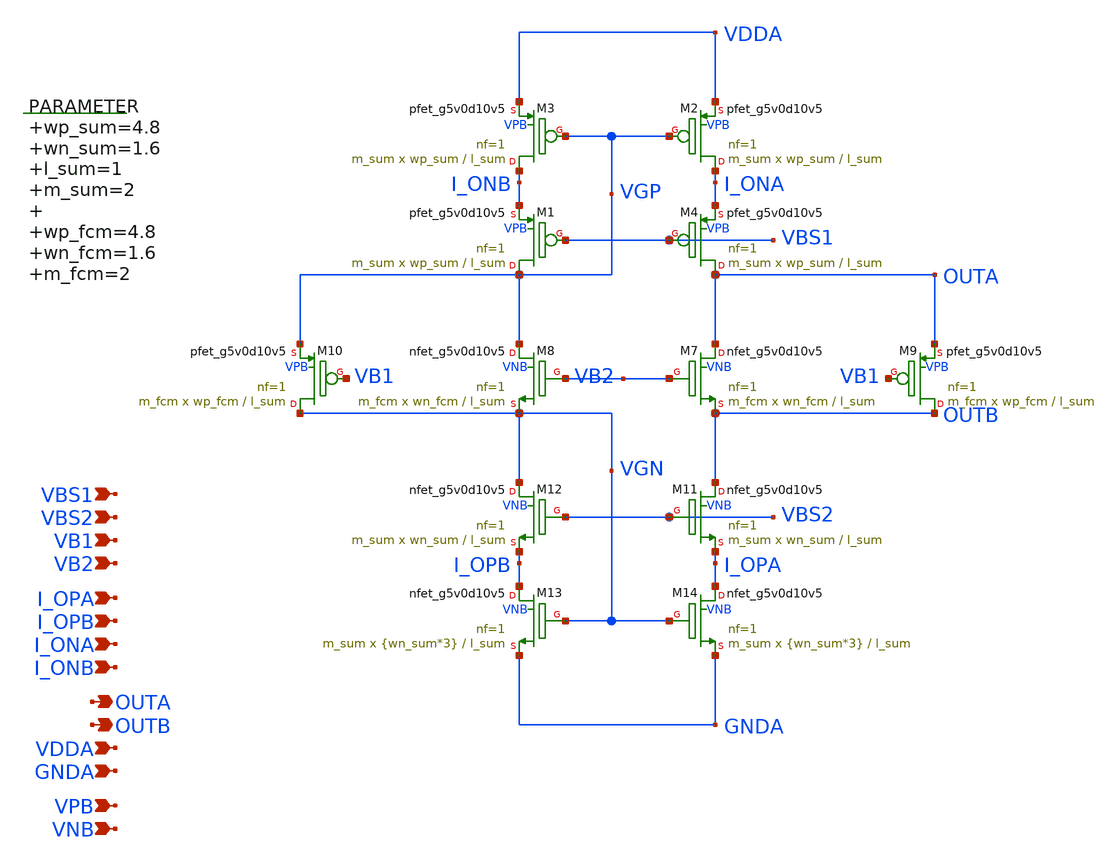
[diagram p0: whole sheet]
** sch_path: xschem/folded_cascode.sch
**.subckt folded_cascode I_OPA I_OPB I_ONA I_ONB OUTA OUTB VBS1 VBS2 VB1 VB2 VDDA VPB GNDA VNB
*.ipin I_OPA
*.ipin I_OPB
*.ipin I_ONA
*.ipin I_ONB
*.opin OUTA
*.opin OUTB
*.ipin VBS1
*.ipin VBS2
*.ipin VB1
*.ipin VB2
*.ipin VDDA
*.ipin VPB
*.ipin GNDA
*.ipin VNB
.param wp_sum=4.8 wn_sum=1.6 l_sum=1 m_sum=2 wp_fcm=4.8 wn_fcm=1.6 m_fcm=2

XM3 I_ONB VGP VDDA VPB sky130_fd_pr__pfet_g5v0d10v5 L=l_sum W=wp_sum nf=1 ad='int((nf+1)/2) * W/nf * 0.29'
+ as='int((nf+2)/2) * W/nf * 0.29' pd='2*int((nf+1)/2) * (W/nf + 0.29)' ps='2*int((nf+2)/2) * (W/nf + 0.29)'
+ nrd='0.29 / W' nrs='0.29 / W' sa=0 sb=0 sd=0 mult=m_sum m=m_sum
XM7 OUTA VB2 OUTB VNB sky130_fd_pr__nfet_g5v0d10v5 L=l_sum W=wn_fcm nf=1 ad='int((nf+1)/2) * W/nf * 0.29'
+ as='int((nf+2)/2) * W/nf * 0.29' pd='2*int((nf+1)/2) * (W/nf + 0.29)' ps='2*int((nf+2)/2) * (W/nf + 0.29)'
+ nrd='0.29 / W' nrs='0.29 / W' sa=0 sb=0 sd=0 mult=m_fcm m=m_fcm
XM8 VGP VB2 VGN VNB sky130_fd_pr__nfet_g5v0d10v5 L=l_sum W=wn_fcm nf=1 ad='int((nf+1)/2) * W/nf * 0.29'
+ as='int((nf+2)/2) * W/nf * 0.29' pd='2*int((nf+1)/2) * (W/nf + 0.29)' ps='2*int((nf+2)/2) * (W/nf + 0.29)'
+ nrd='0.29 / W' nrs='0.29 / W' sa=0 sb=0 sd=0 mult=m_fcm m=m_fcm
XM10 VGN VB1 VGP VPB sky130_fd_pr__pfet_g5v0d10v5 L=l_sum W=wp_fcm nf=1 ad='int((nf+1)/2) * W/nf * 0.29'
+ as='int((nf+2)/2) * W/nf * 0.29' pd='2*int((nf+1)/2) * (W/nf + 0.29)' ps='2*int((nf+2)/2) * (W/nf + 0.29)'
+ nrd='0.29 / W' nrs='0.29 / W' sa=0 sb=0 sd=0 mult=m_fcm m=m_fcm
XM9 OUTB VB1 OUTA VPB sky130_fd_pr__pfet_g5v0d10v5 L=l_sum W=wp_fcm nf=1 ad='int((nf+1)/2) * W/nf * 0.29'
+ as='int((nf+2)/2) * W/nf * 0.29' pd='2*int((nf+1)/2) * (W/nf + 0.29)' ps='2*int((nf+2)/2) * (W/nf + 0.29)'
+ nrd='0.29 / W' nrs='0.29 / W' sa=0 sb=0 sd=0 mult=m_fcm m=m_fcm
XM12 VGN VBS2 I_OPB VNB sky130_fd_pr__nfet_g5v0d10v5 L=l_sum W=wn_sum nf=1 ad='int((nf+1)/2) * W/nf * 0.29'
+ as='int((nf+2)/2) * W/nf * 0.29' pd='2*int((nf+1)/2) * (W/nf + 0.29)' ps='2*int((nf+2)/2) * (W/nf + 0.29)'
+ nrd='0.29 / W' nrs='0.29 / W' sa=0 sb=0 sd=0 mult=m_sum m=m_sum
XM11 OUTB VBS2 I_OPA VNB sky130_fd_pr__nfet_g5v0d10v5 L=l_sum W=wn_sum nf=1 ad='int((nf+1)/2) * W/nf * 0.29'
+ as='int((nf+2)/2) * W/nf * 0.29' pd='2*int((nf+1)/2) * (W/nf + 0.29)' ps='2*int((nf+2)/2) * (W/nf + 0.29)'
+ nrd='0.29 / W' nrs='0.29 / W' sa=0 sb=0 sd=0 mult=m_sum m=m_sum
XM13 I_OPB VGN GNDA VNB sky130_fd_pr__nfet_g5v0d10v5 L=l_sum W={wn_sum*3} nf=1 ad='int((nf+1)/2) * W/nf * 0.29'
+ as='int((nf+2)/2) * W/nf * 0.29' pd='2*int((nf+1)/2) * (W/nf + 0.29)' ps='2*int((nf+2)/2) * (W/nf + 0.29)'
+ nrd='0.29 / W' nrs='0.29 / W' sa=0 sb=0 sd=0 mult=m_sum m=m_sum
XM14 I_OPA VGN GNDA VNB sky130_fd_pr__nfet_g5v0d10v5 L=l_sum W={wn_sum*3} nf=1 ad='int((nf+1)/2) * W/nf * 0.29'
+ as='int((nf+2)/2) * W/nf * 0.29' pd='2*int((nf+1)/2) * (W/nf + 0.29)' ps='2*int((nf+2)/2) * (W/nf + 0.29)'
+ nrd='0.29 / W' nrs='0.29 / W' sa=0 sb=0 sd=0 mult=m_sum m=m_sum
XM1 VGP VBS1 I_ONB VPB sky130_fd_pr__pfet_g5v0d10v5 L=l_sum W=wp_sum nf=1 ad='int((nf+1)/2) * W/nf * 0.29'
+ as='int((nf+2)/2) * W/nf * 0.29' pd='2*int((nf+1)/2) * (W/nf + 0.29)' ps='2*int((nf+2)/2) * (W/nf + 0.29)'
+ nrd='0.29 / W' nrs='0.29 / W' sa=0 sb=0 sd=0 mult=m_sum m=m_sum
XM2 I_ONA VGP VDDA VPB sky130_fd_pr__pfet_g5v0d10v5 L=l_sum W=wp_sum nf=1 ad='int((nf+1)/2) * W/nf * 0.29'
+ as='int((nf+2)/2) * W/nf * 0.29' pd='2*int((nf+1)/2) * (W/nf + 0.29)' ps='2*int((nf+2)/2) * (W/nf + 0.29)'
+ nrd='0.29 / W' nrs='0.29 / W' sa=0 sb=0 sd=0 mult=m_sum m=m_sum
XM4 OUTA VBS1 I_ONA VPB sky130_fd_pr__pfet_g5v0d10v5 L=l_sum W=wp_sum nf=1 ad='int((nf+1)/2) * W/nf * 0.29'
+ as='int((nf+2)/2) * W/nf * 0.29' pd='2*int((nf+1)/2) * (W/nf + 0.29)' ps='2*int((nf+2)/2) * (W/nf + 0.29)'
+ nrd='0.29 / W' nrs='0.29 / W' sa=0 sb=0 sd=0 mult=m_sum m=m_sum
**.ends
.end
